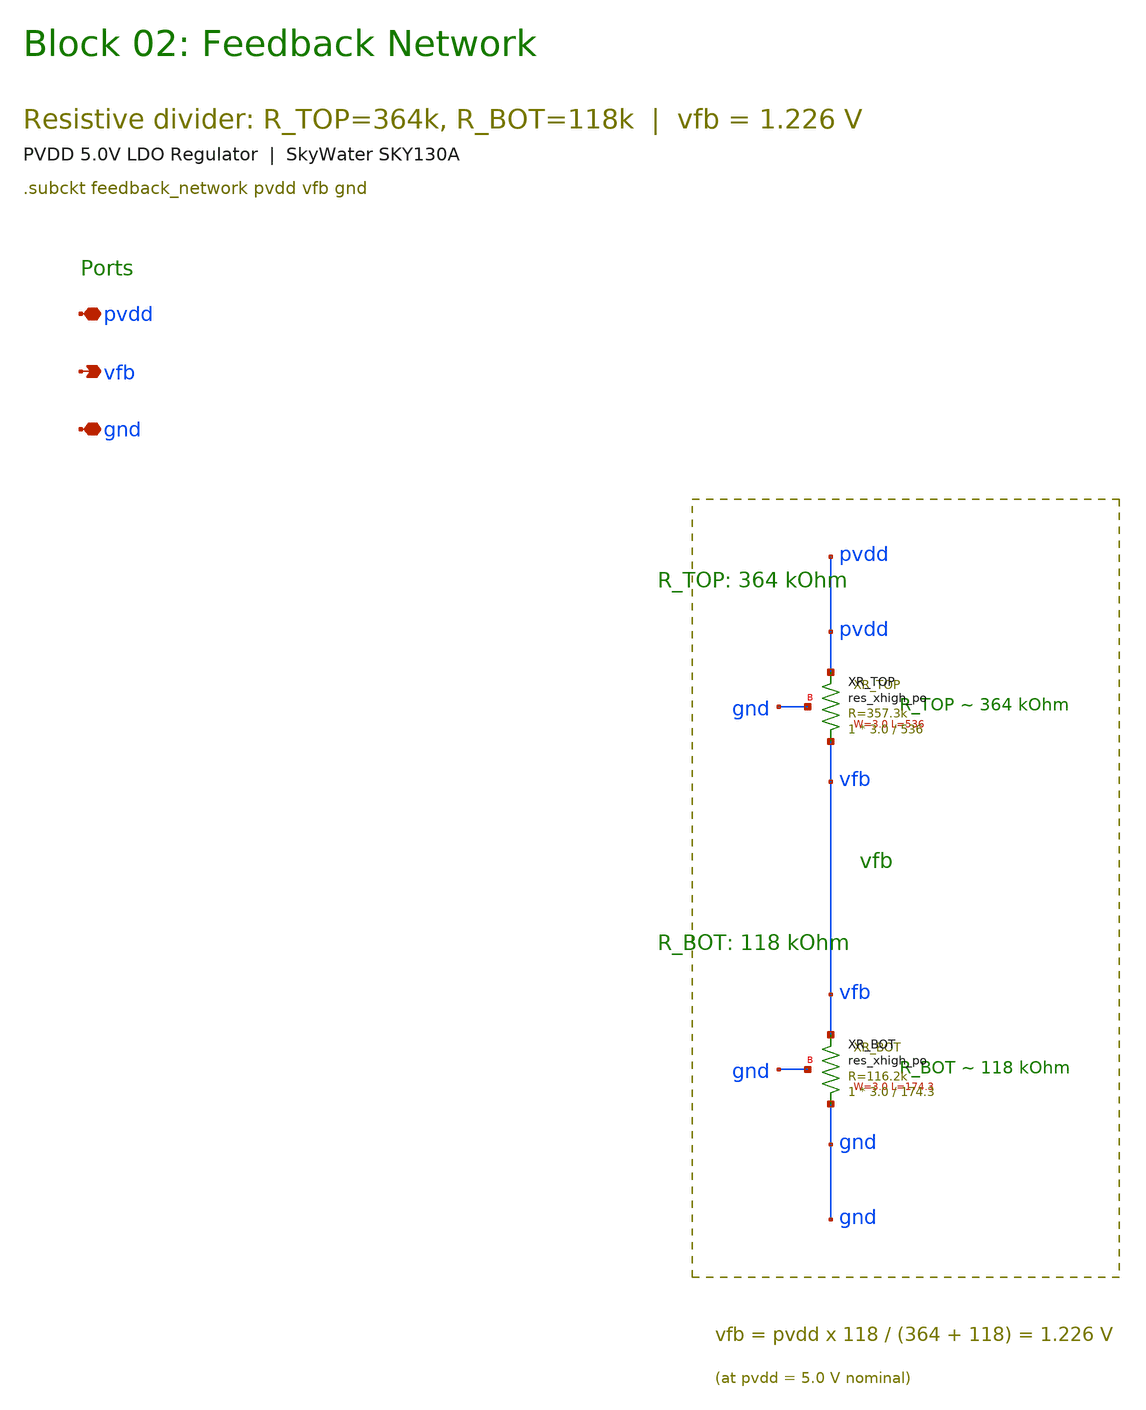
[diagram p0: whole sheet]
** sch_path: pvdd_regulator/10_top_integration/schematics/pvdd_02_feedback.sch
**.subckt pvdd_02_feedback pvdd vfb gnd
*.iopin pvdd
*.opin vfb
*.iopin gnd
XXR_TOP vfb pvdd gnd sky130_fd_pr__res_xhigh_po W=3.0 L=536 mult=1 m=1
XXR_BOT gnd vfb gnd sky130_fd_pr__res_xhigh_po W=3.0 L=174.3 mult=1 m=1
**.ends
.end
